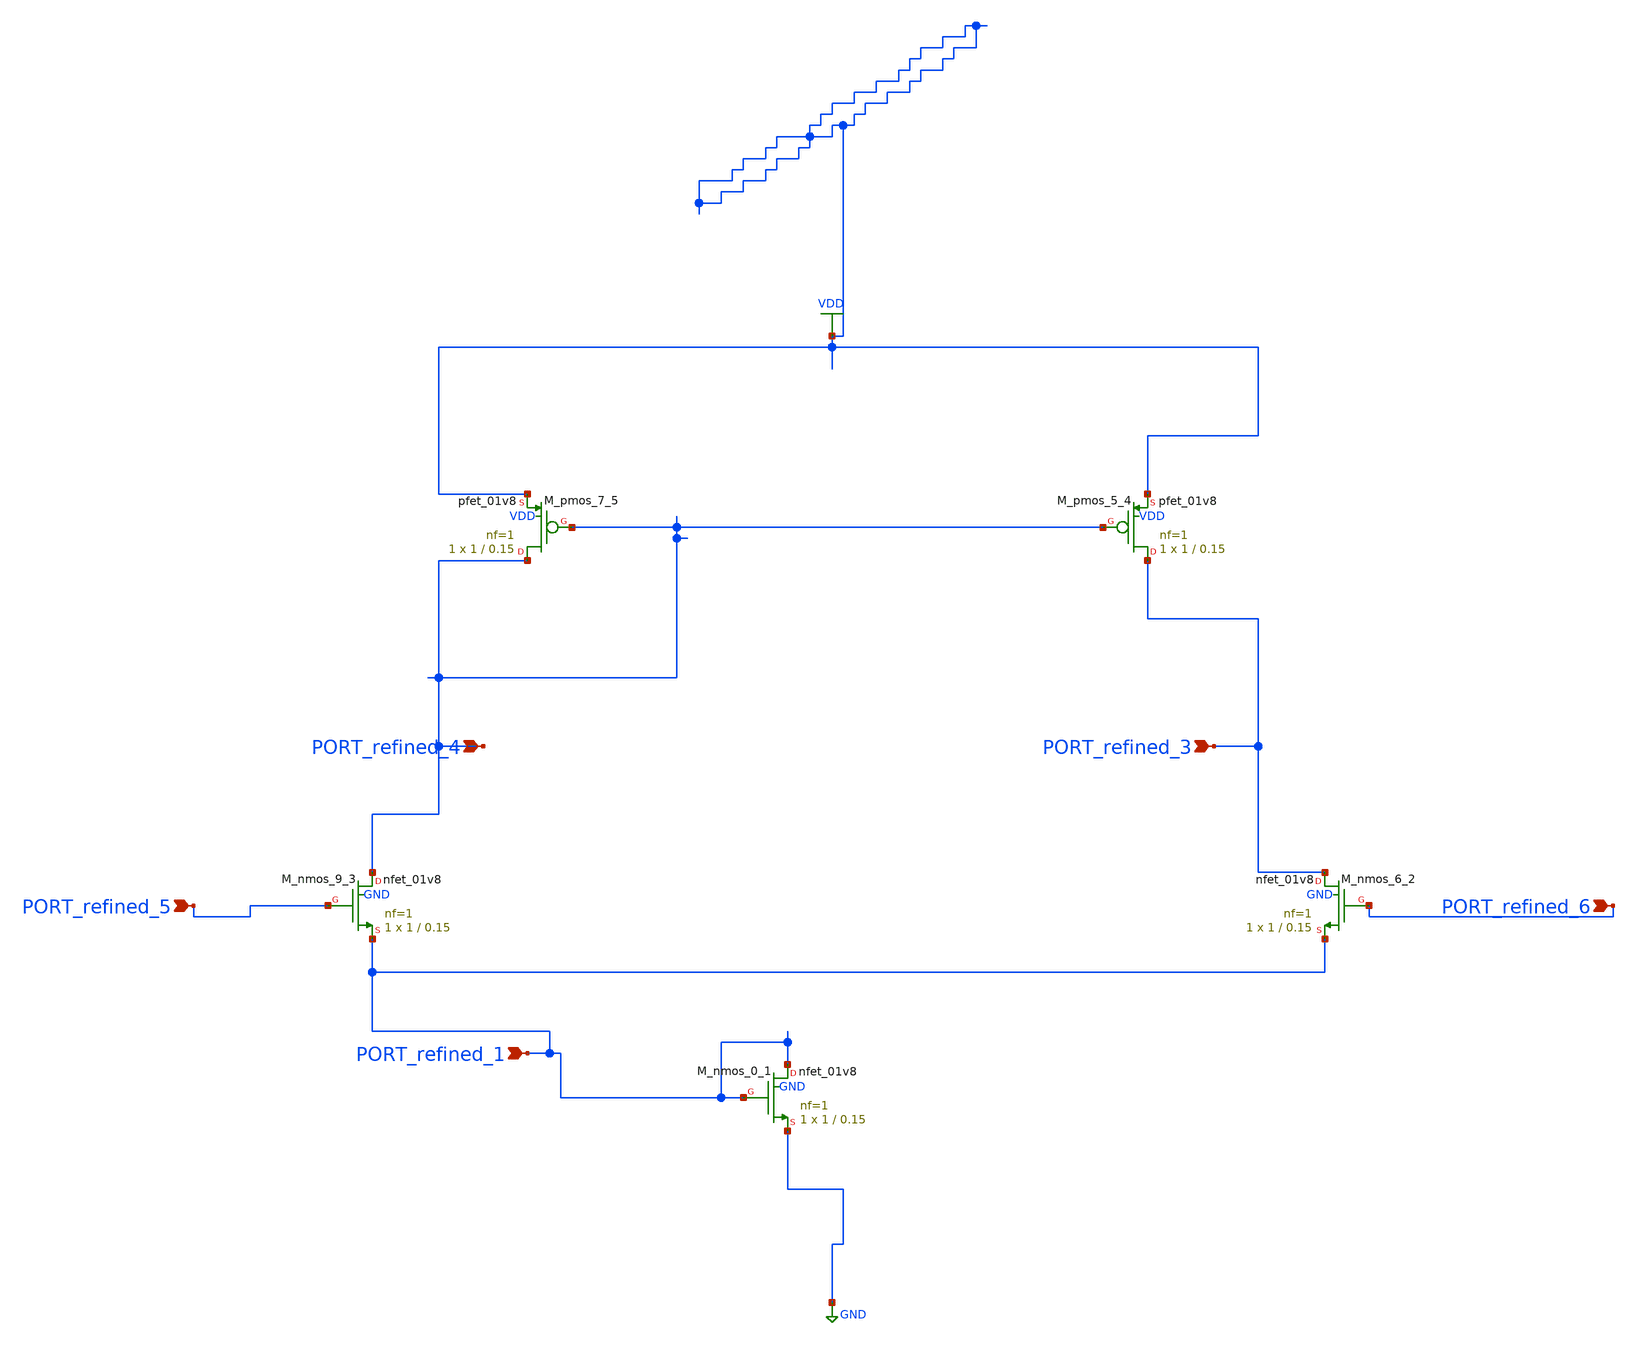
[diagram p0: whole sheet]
** sch_path: schematics/SchemGen/p01_fig1_differential.sch
**.subckt p01_fig1_differential PORT_refined_5 PORT_refined_1 PORT_refined_6 PORT_refined_4
*+ PORT_refined_3
*.ipin PORT_refined_5
*.ipin PORT_refined_1
*.ipin PORT_refined_6
*.ipin PORT_refined_4
*.ipin PORT_refined_3
XM_nmos_0_1 PORT_refined_1 PORT_refined_1 GND GND sky130_fd_pr__nfet_01v8 L=0.15 W=1 nf=1 ad='int((1 + 1)/2) * 1 / 1 * 0.29'
+ as='int((1 + 2)/2) * 1 / 1 * 0.29' pd='2*int((1 + 1)/2) * (1 / 1 + 0.29)' ps='2*int((1 + 2)/2) * (1 / 1 + 0.29)'
+ nrd='0.29 / 1 ' nrs='0.29 / 1 ' sa=0 sb=0 sd=0 mult=1 m=1
XM_nmos_6_2 PORT_refined_3 PORT_refined_6 PORT_refined_1 GND sky130_fd_pr__nfet_01v8 L=0.15 W=1 nf=1
+ ad='int((1 + 1)/2) * 1 / 1 * 0.29' as='int((1 + 2)/2) * 1 / 1 * 0.29' pd='2*int((1 + 1)/2) * (1 / 1 + 0.29)'
+ ps='2*int((1 + 2)/2) * (1 / 1 + 0.29)' nrd='0.29 / 1 ' nrs='0.29 / 1 ' sa=0 sb=0 sd=0 mult=1 m=1
XM_nmos_9_3 PORT_refined_4 PORT_refined_5 PORT_refined_1 GND sky130_fd_pr__nfet_01v8 L=0.15 W=1 nf=1
+ ad='int((1 + 1)/2) * 1 / 1 * 0.29' as='int((1 + 2)/2) * 1 / 1 * 0.29' pd='2*int((1 + 1)/2) * (1 / 1 + 0.29)'
+ ps='2*int((1 + 2)/2) * (1 / 1 + 0.29)' nrd='0.29 / 1 ' nrs='0.29 / 1 ' sa=0 sb=0 sd=0 mult=1 m=1
XM_pmos_5_4 PORT_refined_3 PORT_refined_4 VDD VDD sky130_fd_pr__pfet_01v8 L=0.15 W=1 nf=1 ad='int((1 + 1)/2) * 1 / 1 * 0.29'
+ as='int((1 + 2)/2) * 1 / 1 * 0.29' pd='2*int((1 + 1)/2) * (1 / 1 + 0.29)' ps='2*int((1 + 2)/2) * (1 / 1 + 0.29)'
+ nrd='0.29 / 1 ' nrs='0.29 / 1 ' sa=0 sb=0 sd=0 mult=1 m=1
XM_pmos_7_5 PORT_refined_4 PORT_refined_4 VDD VDD sky130_fd_pr__pfet_01v8 L=0.15 W=1 nf=1 ad='int((1 + 1)/2) * 1 / 1 * 0.29'
+ as='int((1 + 2)/2) * 1 / 1 * 0.29' pd='2*int((1 + 1)/2) * (1 / 1 + 0.29)' ps='2*int((1 + 2)/2) * (1 / 1 + 0.29)'
+ nrd='0.29 / 1 ' nrs='0.29 / 1 ' sa=0 sb=0 sd=0 mult=1 m=1
**.ends
.GLOBAL GND
.GLOBAL VDD
.end
